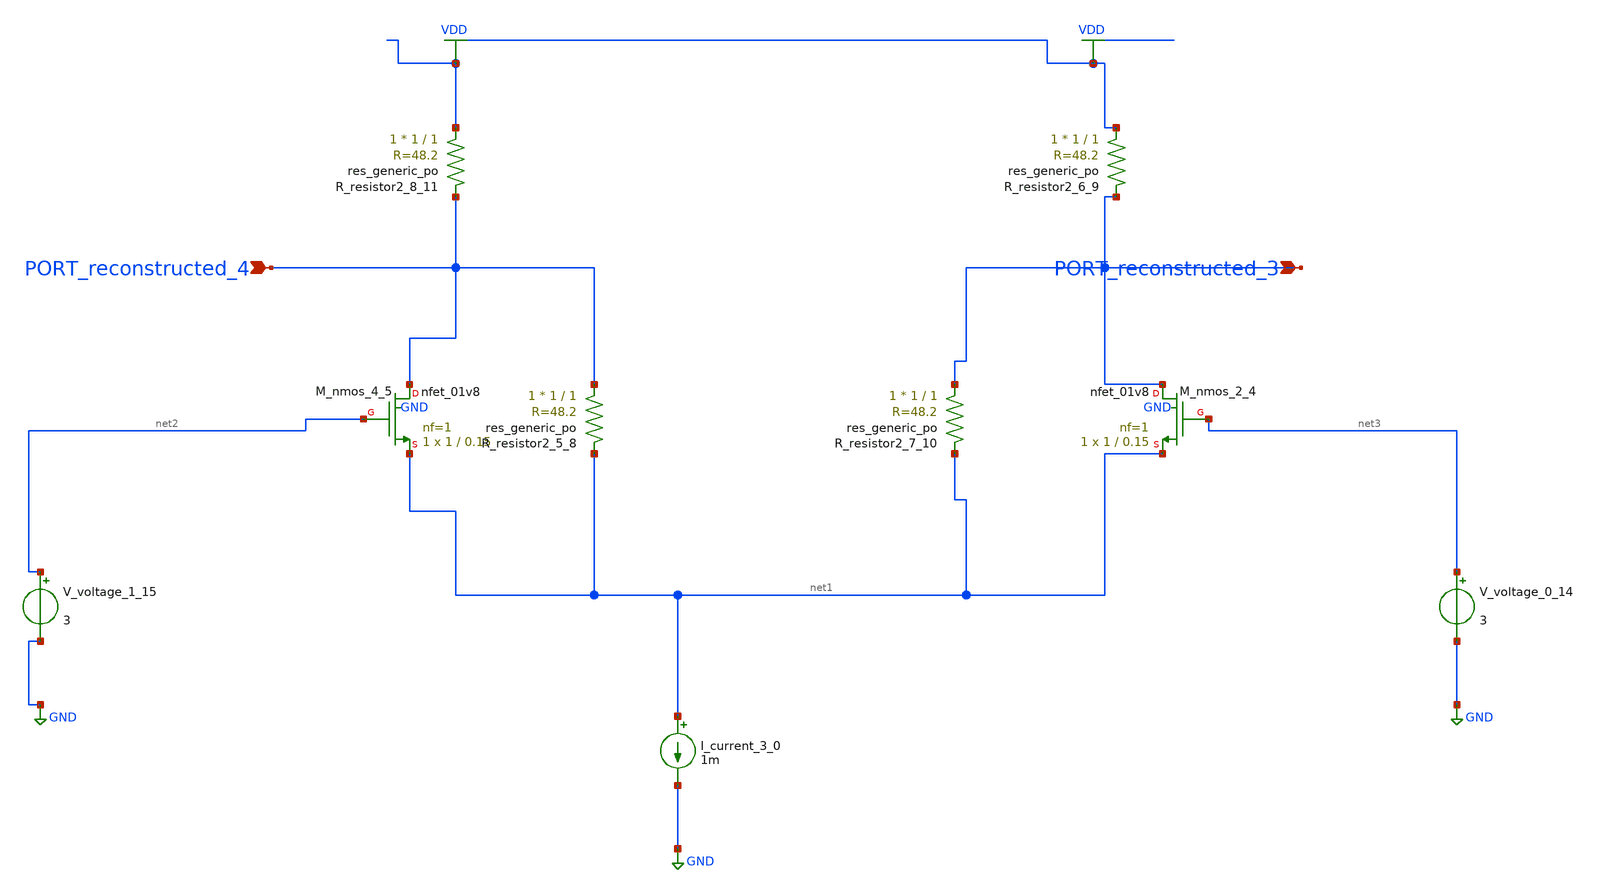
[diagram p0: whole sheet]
** sch_path: schematics/AMSNet/206.sch
**.subckt 206 PORT_reconstructed_3 PORT_reconstructed_4
*.ipin PORT_reconstructed_3
*.ipin PORT_reconstructed_4
I_current_3_0 net1 GND 1m
XM_nmos_2_4 PORT_reconstructed_3 net3 net1 GND sky130_fd_pr__nfet_01v8 L=0.15 W=1 nf=1 ad='int((1 + 1)/2) * 1 / 1 * 0.29'
+ as='int((1 + 2)/2) * 1 / 1 * 0.29' pd='2*int((1 + 1)/2) * (1 / 1 + 0.29)' ps='2*int((1 + 2)/2) * (1 / 1 + 0.29)'
+ nrd='0.29 / 1 ' nrs='0.29 / 1 ' sa=0 sb=0 sd=0 mult=1 m=1
XM_nmos_4_5 PORT_reconstructed_4 net2 net1 GND sky130_fd_pr__nfet_01v8 L=0.15 W=1 nf=1 ad='int((1 + 1)/2) * 1 / 1 * 0.29'
+ as='int((1 + 2)/2) * 1 / 1 * 0.29' pd='2*int((1 + 1)/2) * (1 / 1 + 0.29)' ps='2*int((1 + 2)/2) * (1 / 1 + 0.29)'
+ nrd='0.29 / 1 ' nrs='0.29 / 1 ' sa=0 sb=0 sd=0 mult=1 m=1
XR_resistor2_5_8 PORT_reconstructed_4 net1 sky130_fd_pr__res_generic_po W=1 L=1 m=1
XR_resistor2_6_9 VDD PORT_reconstructed_3 sky130_fd_pr__res_generic_po W=1 L=1 m=1
XR_resistor2_7_10 PORT_reconstructed_3 net1 sky130_fd_pr__res_generic_po W=1 L=1 m=1
XR_resistor2_8_11 VDD PORT_reconstructed_4 sky130_fd_pr__res_generic_po W=1 L=1 m=1
V_voltage_0_14 net3 GND 3
V_voltage_1_15 net2 GND 3
**.ends
.GLOBAL GND
.GLOBAL VDD
.end
